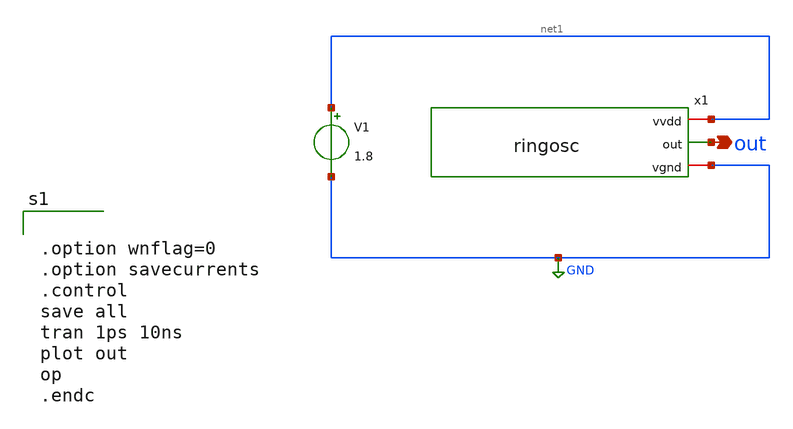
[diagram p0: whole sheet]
** sch_path: ringosc-tb.sch
**.subckt ringosc-tb out
*.opin out
V1 net1 GND 1.8
x1 net1 out GND ringosc
**** begin user architecture code

** opencircuitdesign pdks install
.lib $::SKYWATER_MODELS/sky130.lib.spice tt




.option wnflag=0
.option savecurrents
.control
save all
tran 1ps 10ns
plot out
op
.endc


**** end user architecture code
**.ends

* expanding   symbol:  ringosc.sym # of pins=3
** sym_path: ringosc.sym
** sch_path: ringosc.sch
.subckt ringosc vvdd out vgnd
*.iopin vvdd
*.iopin vgnd
*.opin out
x1 vvdd net2 net1 vgnd inverter
x2 vvdd out net2 vgnd inverter
x3 vvdd net1 out vgnd inverter
.ends


* expanding   symbol:  inverter.sym # of pins=4
** sym_path: inverter.sym
** sch_path: inverter.sch
.subckt inverter vvdd out in vgnd
*.ipin in
*.opin out
*.iopin vvdd
*.iopin vgnd
XM1 out in vgnd vgnd sky130_fd_pr__nfet_01v8 L=0.15 W=1 nf=1 ad='int((nf+1)/2) * W/nf * 0.29' as='int((nf+2)/2) * W/nf * 0.29'
+ pd='2*int((nf+1)/2) * (W/nf + 0.29)' ps='2*int((nf+2)/2) * (W/nf + 0.29)' nrd='0.29 / W' nrs='0.29 / W'
+ sa=0 sb=0 sd=0 mult=1 m=1
XM2 out in vvdd vvdd sky130_fd_pr__pfet_01v8 L=0.15 W=1 nf=1 ad='int((nf+1)/2) * W/nf * 0.29' as='int((nf+2)/2) * W/nf * 0.29'
+ pd='2*int((nf+1)/2) * (W/nf + 0.29)' ps='2*int((nf+2)/2) * (W/nf + 0.29)' nrd='0.29 / W' nrs='0.29 / W'
+ sa=0 sb=0 sd=0 mult=1 m=1
.ends

.GLOBAL GND
.end
